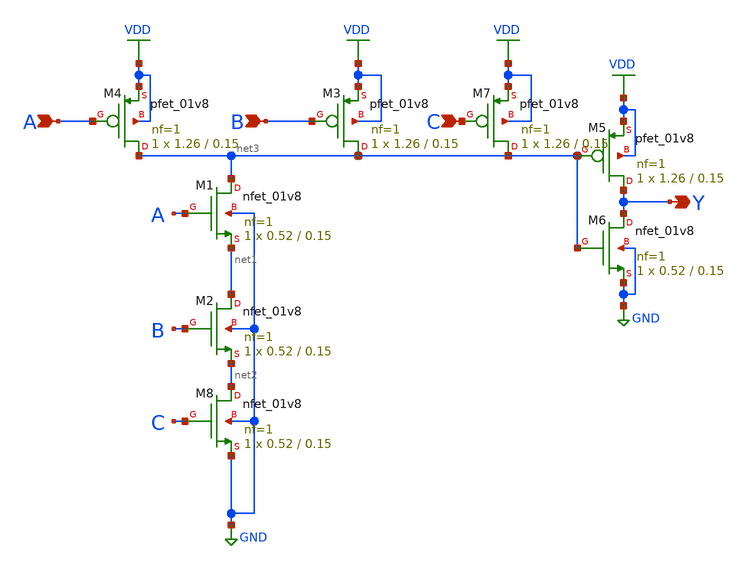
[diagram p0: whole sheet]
** sch_path: xschem/and31.sch
**.subckt and31 B A Y C
*.ipin B
*.ipin A
*.opin Y
*.ipin C
XM1 net3 A net1 GND sky130_fd_pr__nfet_01v8 L=0.15 W=0.52 nf=1 ad='int((nf+1)/2) * W/nf * 0.29' as='int((nf+2)/2) * W/nf * 0.29'
+ pd='2*int((nf+1)/2) * (W/nf + 0.29)' ps='2*int((nf+2)/2) * (W/nf + 0.29)' nrd='0.29 / W' nrs='0.29 / W'
+ sa=0 sb=0 sd=0 mult=1 m=1
XM2 net1 B net2 GND sky130_fd_pr__nfet_01v8 L=0.15 W=0.52 nf=1 ad='int((nf+1)/2) * W/nf * 0.29' as='int((nf+2)/2) * W/nf * 0.29'
+ pd='2*int((nf+1)/2) * (W/nf + 0.29)' ps='2*int((nf+2)/2) * (W/nf + 0.29)' nrd='0.29 / W' nrs='0.29 / W'
+ sa=0 sb=0 sd=0 mult=1 m=1
XM3 net3 B VDD VDD sky130_fd_pr__pfet_01v8 L=0.15 W=1.26 nf=1 ad='int((nf+1)/2) * W/nf * 0.29' as='int((nf+2)/2) * W/nf * 0.29'
+ pd='2*int((nf+1)/2) * (W/nf + 0.29)' ps='2*int((nf+2)/2) * (W/nf + 0.29)' nrd='0.29 / W' nrs='0.29 / W'
+ sa=0 sb=0 sd=0 mult=1 m=1
XM4 net3 A VDD VDD sky130_fd_pr__pfet_01v8 L=0.15 W=1.26 nf=1 ad='int((nf+1)/2) * W/nf * 0.29' as='int((nf+2)/2) * W/nf * 0.29'
+ pd='2*int((nf+1)/2) * (W/nf + 0.29)' ps='2*int((nf+2)/2) * (W/nf + 0.29)' nrd='0.29 / W' nrs='0.29 / W'
+ sa=0 sb=0 sd=0 mult=1 m=1
XM5 Y net3 VDD VDD sky130_fd_pr__pfet_01v8 L=0.15 W=1.26 nf=1 ad='int((nf+1)/2) * W/nf * 0.29' as='int((nf+2)/2) * W/nf * 0.29'
+ pd='2*int((nf+1)/2) * (W/nf + 0.29)' ps='2*int((nf+2)/2) * (W/nf + 0.29)' nrd='0.29 / W' nrs='0.29 / W'
+ sa=0 sb=0 sd=0 mult=1 m=1
XM6 Y net3 GND GND sky130_fd_pr__nfet_01v8 L=0.15 W=0.52 nf=1 ad='int((nf+1)/2) * W/nf * 0.29' as='int((nf+2)/2) * W/nf * 0.29'
+ pd='2*int((nf+1)/2) * (W/nf + 0.29)' ps='2*int((nf+2)/2) * (W/nf + 0.29)' nrd='0.29 / W' nrs='0.29 / W'
+ sa=0 sb=0 sd=0 mult=1 m=1
XM7 net3 C VDD VDD sky130_fd_pr__pfet_01v8 L=0.15 W=1.26 nf=1 ad='int((nf+1)/2) * W/nf * 0.29' as='int((nf+2)/2) * W/nf * 0.29'
+ pd='2*int((nf+1)/2) * (W/nf + 0.29)' ps='2*int((nf+2)/2) * (W/nf + 0.29)' nrd='0.29 / W' nrs='0.29 / W'
+ sa=0 sb=0 sd=0 mult=1 m=1
XM8 net2 C GND GND sky130_fd_pr__nfet_01v8 L=0.15 W=0.52 nf=1 ad='int((nf+1)/2) * W/nf * 0.29' as='int((nf+2)/2) * W/nf * 0.29'
+ pd='2*int((nf+1)/2) * (W/nf + 0.29)' ps='2*int((nf+2)/2) * (W/nf + 0.29)' nrd='0.29 / W' nrs='0.29 / W'
+ sa=0 sb=0 sd=0 mult=1 m=1
**.ends
.GLOBAL GND
.GLOBAL VDD
.end
